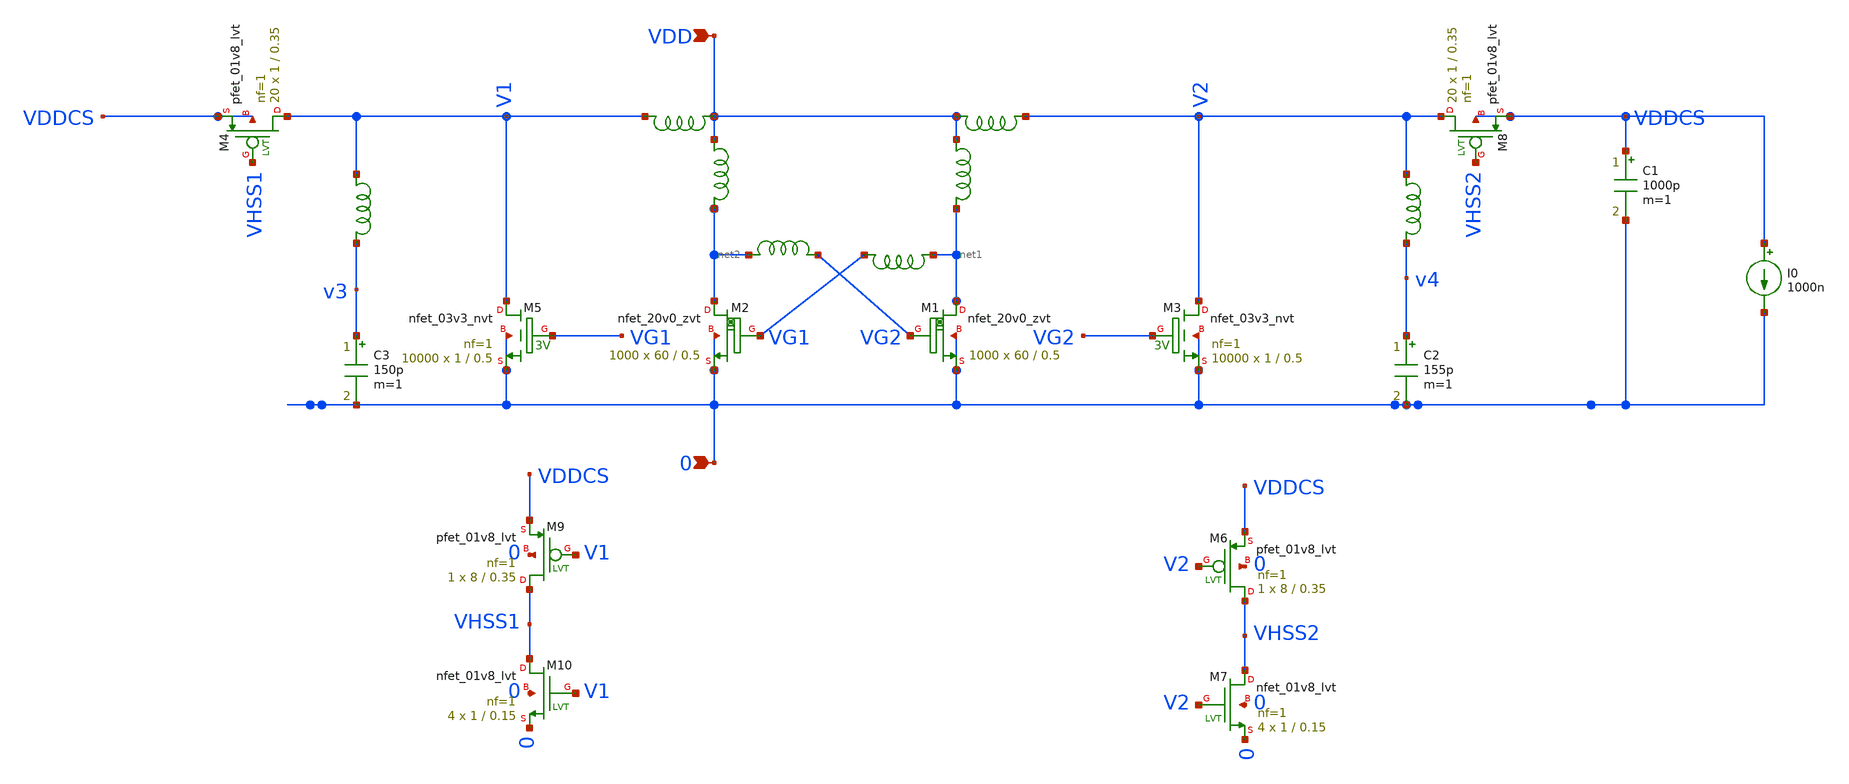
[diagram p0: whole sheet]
** sch_path: design/LELO_SVOD_SKY130A/LELO_EXSC.sch
**.subckt LELO_EXSC 0 VDD
*.ipin 0
*.ipin VDD
x3 VDD net1 1812PS-102_imp
x4 VDD net2 1812PS-102_imp
XM1 net1 VG2 0 0 sky130_fd_pr__nfet_20v0_zvt W=60 L=0.5 m=1000
XM2 net2 VG1 0 0 sky130_fd_pr__nfet_20v0_zvt W=60 L=0.5 m=1000
x1 net2 VG2 1812PS-104_imp
x2 net1 VG1 1812PS-104_imp
C1 VDDCS 0 1000p m=1
XM4 V1 VHSS1 VDDCS VDDCS sky130_fd_pr__pfet_01v8_lvt L=0.35 W=1 nf=1 ad='int((1 + 1)/2) * 1 / 1 * 0.29'
+ as='int((1 + 2)/2) * 1 / 1 * 0.29' pd='2*int((1 + 1)/2) * (1 / 1 + 0.29)' ps='2*int((1 + 2)/2) * (1 / 1 + 0.29)'
+ nrd='0.29 / 1 ' nrs='0.29 / 1 ' sa=0 sb=0 sd=0 mult=20 m=20
XM3 V2 VG2 0 0 sky130_fd_pr__nfet_03v3_nvt L=0.5 W=1 nf=1 ad='int((1 + 1)/2) * 1 / 1 * 0.29' as='int((1 + 2)/2) * 1 / 1 * 0.29'
+ pd='2*int((1 + 1)/2) * (1 / 1 + 0.29)' ps='2*int((1 + 2)/2) * (1 / 1 + 0.29)' nrd='0.29 / 1 ' nrs='0.29 / 1 '
+ sa=0 sb=0 sd=0 mult=10000 m=10000
XM5 V1 VG1 0 0 sky130_fd_pr__nfet_03v3_nvt L=0.5 W=1 nf=1 ad='int((1 + 1)/2) * 1 / 1 * 0.29' as='int((1 + 2)/2) * 1 / 1 * 0.29'
+ pd='2*int((1 + 1)/2) * (1 / 1 + 0.29)' ps='2*int((1 + 2)/2) * (1 / 1 + 0.29)' nrd='0.29 / 1 ' nrs='0.29 / 1 '
+ sa=0 sb=0 sd=0 mult=10000 m=10000
C3 v3 0 150p m=1
x7 V1 v3 1812PS-564_imp
I0 VDDCS 0 1000n
XM8 V2 VHSS2 VDDCS VDDCS sky130_fd_pr__pfet_01v8_lvt L=0.35 W=1 nf=1 ad='int((1 + 1)/2) * 1 / 1 * 0.29'
+ as='int((1 + 2)/2) * 1 / 1 * 0.29' pd='2*int((1 + 1)/2) * (1 / 1 + 0.29)' ps='2*int((1 + 2)/2) * (1 / 1 + 0.29)'
+ nrd='0.29 / 1 ' nrs='0.29 / 1 ' sa=0 sb=0 sd=0 mult=20 m=20
XM6 VHSS2 V2 VDDCS 0 sky130_fd_pr__pfet_01v8_lvt L=0.35 W=8 nf=1 ad='int((1 + 1)/2) * 8 / 1 * 0.29' as='int((1 + 2)/2) * 8 / 1 * 0.29'
+ pd='2*int((1 + 1)/2) * (8 / 1 + 0.29)' ps='2*int((1 + 2)/2) * (8 / 1 + 0.29)' nrd='0.29 / 8 ' nrs='0.29 / 8 '
+ sa=0 sb=0 sd=0 mult=1 m=1
XM7 VHSS2 V2 0 0 sky130_fd_pr__nfet_01v8_lvt L=0.15 W=1 nf=1 ad='int((1 + 1)/2) * 1 / 1 * 0.29' as='int((1 + 2)/2) * 1 / 1 * 0.29'
+ pd='2*int((1 + 1)/2) * (1 / 1 + 0.29)' ps='2*int((1 + 2)/2) * (1 / 1 + 0.29)' nrd='0.29 / 1 ' nrs='0.29 / 1 '
+ sa=0 sb=0 sd=0 mult=4 m=4
XM9 VHSS1 V1 VDDCS 0 sky130_fd_pr__pfet_01v8_lvt L=0.35 W=8 nf=1 ad='int((1 + 1)/2) * 8 / 1 * 0.29' as='int((1 + 2)/2) * 8 / 1 * 0.29'
+ pd='2*int((1 + 1)/2) * (8 / 1 + 0.29)' ps='2*int((1 + 2)/2) * (8 / 1 + 0.29)' nrd='0.29 / 8 ' nrs='0.29 / 8 '
+ sa=0 sb=0 sd=0 mult=1 m=1
XM10 VHSS1 V1 0 0 sky130_fd_pr__nfet_01v8_lvt L=0.15 W=1 nf=1 ad='int((1 + 1)/2) * 1 / 1 * 0.29' as='int((1 + 2)/2) * 1 / 1 * 0.29'
+ pd='2*int((1 + 1)/2) * (1 / 1 + 0.29)' ps='2*int((1 + 2)/2) * (1 / 1 + 0.29)' nrd='0.29 / 1 ' nrs='0.29 / 1 '
+ sa=0 sb=0 sd=0 mult=4 m=4
x5 VDD V1 1812PS-564_imp
x6 V2 v4 1812PS-564_imp
C2 v4 0 155p m=1
x8 V2 VDD 1812PS-564_imp
**.ends

* expanding   symbol:  LELO_SVOD_SKY130A/1812PS-102_imp.sym # of pins=2
** sym_path: design/LELO_SVOD_SKY130A/1812PS-102_imp.sym

.subckt 1812PS-102_imp port1 port2
X1 port1 port2 Model1D R1=60 R2=0.054 C= 0.15p K1=0.000001 K2=0.064 K3= 1u K4=1E-06 K5=0.000001 L=0
+ Is=0 a=0 L_Z0=0 L_EL=0 L_F0=0E6 PkZ=1282.46492
.ends 1812PS-102_imp

* expanding   symbol:  LELO_SVOD_SKY130A/1812PS-104_imp.sym # of pins=2
** sym_path: design/LELO_SVOD_SKY130A/1812PS-104_imp.sym

.subckt 1812PS-104_imp port1 port2
X1 port1 port2 Model1D R1=40 R2=1.3 C= 1.6p K1=0.000001 K2=13.98 K3= 100u K4=0.000001 K5=0.000001
+ L=0 Is=0 a=0 L_Z0=0 L_EL=0 L_F0=0E6 PkZ=48065.0165
.ends 1812PS-104_imp

* expanding   symbol:  LELO_SVOD_SKY130A/1812PS-564_imp.sym # of pins=2
** sym_path: design/LELO_SVOD_SKY130A/1812PS-564_imp.sym

.subckt 1812PS-564_imp port1 port2
X1 port1 port2 Model1D R1=70 R2=6.1 C= 7.71p K1=0.000001 K2=115.8 K3= 560u K4=0.000001 K5=0.000001
+ L=0 Is=0 a=0 L_Z0=0 L_EL=0 L_F0=0E6 PkZ=153558.837
.ends 1812PS-564_imp
.end
